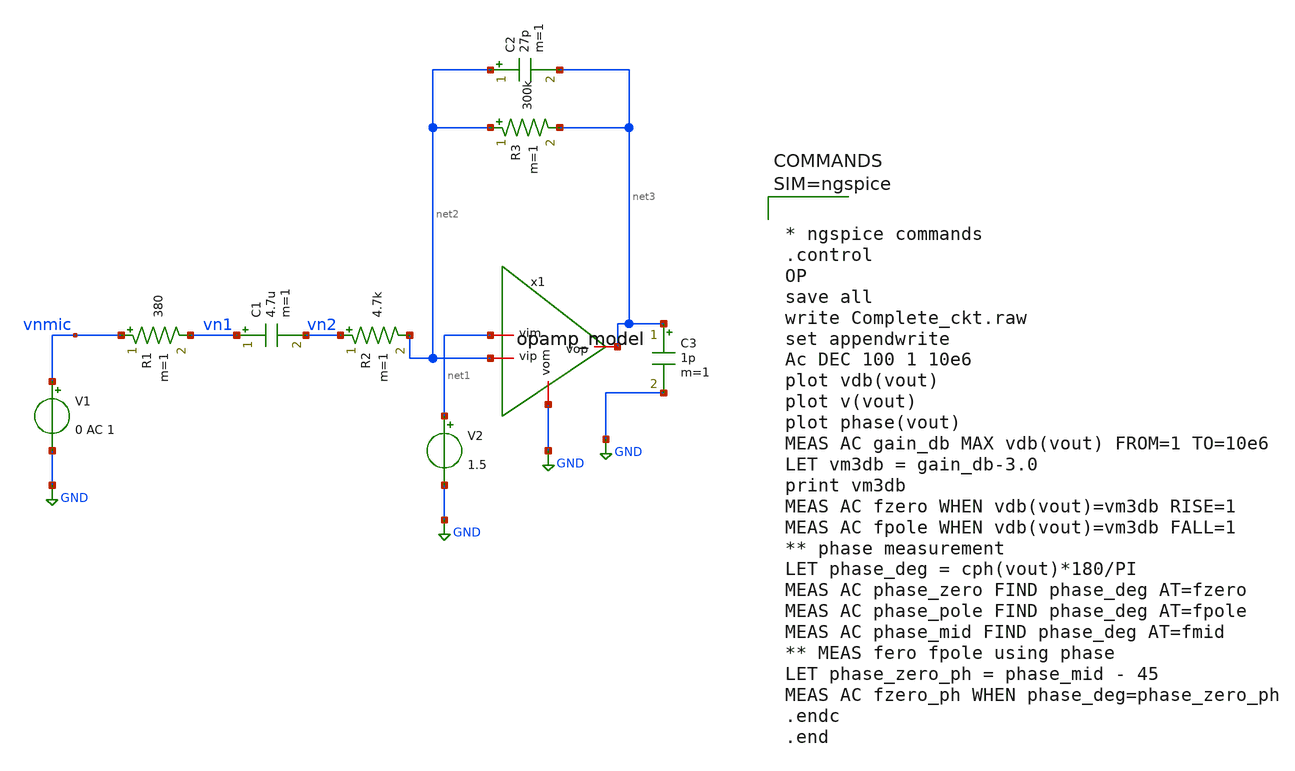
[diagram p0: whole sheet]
** sch_path: xschem/mictestop.sch
**.subckt mictestop
V1 vnmic GND 0 AC 1
R1 vnmic vn1 380 m=1
C1 vn1 vn2 4.7u m=1
R2 vn2 net2 4.7k m=1
R3 net2 net3 300k m=1
C2 net2 net3 27p m=1
C3 net3 GND 1p m=1
V2 net1 GND 1.5
x1 net3 net2 net1 GND opamp_model
**** begin user architecture code



* ngspice commands
.control
OP
save all
write Complete_ckt.raw
set appendwrite
Ac DEC 100 1 10e6
plot vdb(vout)
plot v(vout)
plot phase(vout)
MEAS AC gain_db MAX vdb(vout) FROM=1 TO=10e6
LET vm3db = gain_db-3.0
print vm3db
MEAS AC fzero WHEN vdb(vout)=vm3db RISE=1
MEAS AC fpole WHEN vdb(vout)=vm3db FALL=1
** phase measurement
LET phase_deg = cph(vout)*180/PI
MEAS AC phase_zero FIND phase_deg AT=fzero
MEAS AC phase_pole FIND phase_deg AT=fpole
MEAS AC phase_mid FIND phase_deg AT=fmid
** MEAS fero fpole using phase
LET phase_zero_ph = phase_mid - 45
MEAS AC fzero_ph WHEN phase_deg=phase_zero_ph
.endc
.end



**** end user architecture code
**.ends

* expanding   symbol:  opamp_model.sym # of pins=4
** sym_path: xschem/opamp_model.sym
** sch_path: xschem/opamp_model.sch
.subckt opamp_model vop vip vim vom
*.iopin vop
*.iopin vom
*.iopin vip
*.iopin vim
E1 vop vom vip vim 1000
.ends

.GLOBAL GND
.end
